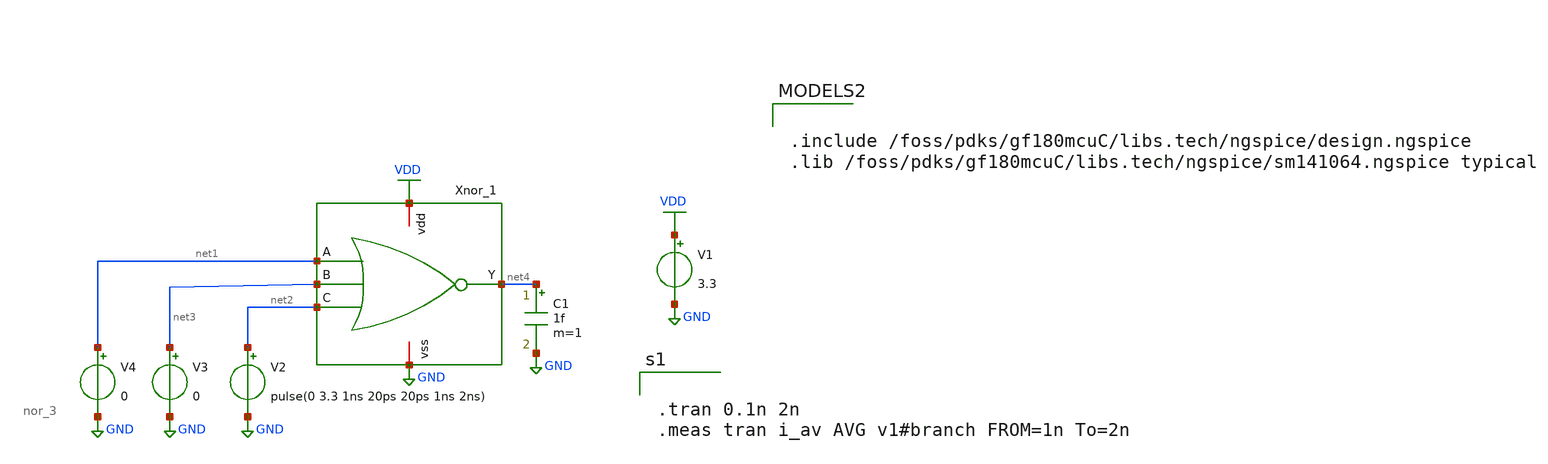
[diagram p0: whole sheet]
** sch_path: Cells/NOR3_1/nor_3_tb.sch
**.subckt nor_3_tb
V1 VDD GND 3.3
V2 net2 GND pulse(0 3.3 1ns 20ps 20ps 1ns 2ns)
V3 net3 GND 0
V4 net1 GND 0
Xnor_1 VDD net1 net3 net2 net4 GND nor_3
C1 net4 GND 1f m=1
**** begin user architecture code

.include /foss/pdks/gf180mcuC/libs.tech/ngspice/design.ngspice
.lib /foss/pdks/gf180mcuC/libs.tech/ngspice/sm141064.ngspice typical



.tran 0.1n 2n
.meas tran i_av AVG v1#branch FROM=1n To=2n

**** end user architecture code
**.ends

* expanding   symbol:  nor_3.sym # of pins=6
** sym_path: Cells/NOR3_1/nor_3.sym
** sch_path: Cells/NOR3_1/nor_3.sch
.subckt nor_3 vdd A B C Y vss
*.iopin vdd
*.iopin vss
*.ipin B
*.ipin A
*.ipin C
*.opin Y
XM13 net1 A vdd vdd pfet_03v3 L=0.3u W=2.55u nf=1 ad='int((nf+1)/2) * W/nf * 0.18u' as='int((nf+2)/2) * W/nf * 0.18u'
+ pd='2*int((nf+1)/2) * (W/nf + 0.18u)' ps='2*int((nf+2)/2) * (W/nf + 0.18u)' nrd='0.18u / W' nrs='0.18u / W'
+ sa=0 sb=0 sd=0 m=1
XM14 net2 B net1 vdd pfet_03v3 L=0.3u W=2.55u nf=1 ad='int((nf+1)/2) * W/nf * 0.18u' as='int((nf+2)/2) * W/nf * 0.18u'
+ pd='2*int((nf+1)/2) * (W/nf + 0.18u)' ps='2*int((nf+2)/2) * (W/nf + 0.18u)' nrd='0.18u / W' nrs='0.18u / W'
+ sa=0 sb=0 sd=0 m=1
XM15 Y C net2 vdd pfet_03v3 L=0.3u W=2.55u nf=1 ad='int((nf+1)/2) * W/nf * 0.18u' as='int((nf+2)/2) * W/nf * 0.18u'
+ pd='2*int((nf+1)/2) * (W/nf + 0.18u)' ps='2*int((nf+2)/2) * (W/nf + 0.18u)' nrd='0.18u / W' nrs='0.18u / W'
+ sa=0 sb=0 sd=0 m=1
XM16 Y A vss vss nfet_03v3 L=0.3u W=0.85u nf=1 ad='int((nf+1)/2) * W/nf * 0.18u' as='int((nf+2)/2) * W/nf * 0.18u'
+ pd='2*int((nf+1)/2) * (W/nf + 0.18u)' ps='2*int((nf+2)/2) * (W/nf + 0.18u)' nrd='0.18u / W' nrs='0.18u / W'
+ sa=0 sb=0 sd=0 m=1
XM17 Y B vss vss nfet_03v3 L=0.3u W=0.85u nf=1 ad='int((nf+1)/2) * W/nf * 0.18u' as='int((nf+2)/2) * W/nf * 0.18u'
+ pd='2*int((nf+1)/2) * (W/nf + 0.18u)' ps='2*int((nf+2)/2) * (W/nf + 0.18u)' nrd='0.18u / W' nrs='0.18u / W'
+ sa=0 sb=0 sd=0 m=1
XM18 Y C vss vss nfet_03v3 L=0.3u W=0.85u nf=1 ad='int((nf+1)/2) * W/nf * 0.18u' as='int((nf+2)/2) * W/nf * 0.18u'
+ pd='2*int((nf+1)/2) * (W/nf + 0.18u)' ps='2*int((nf+2)/2) * (W/nf + 0.18u)' nrd='0.18u / W' nrs='0.18u / W'
+ sa=0 sb=0 sd=0 m=1
**** begin user architecture code

.include /foss/pdks/gf180mcuC/libs.tech/ngspice/design.ngspice
.lib /foss/pdks/gf180mcuC/libs.tech/ngspice/sm141064.ngspice typical

**** end user architecture code
.ends

.GLOBAL VDD
.GLOBAL GND
.end
